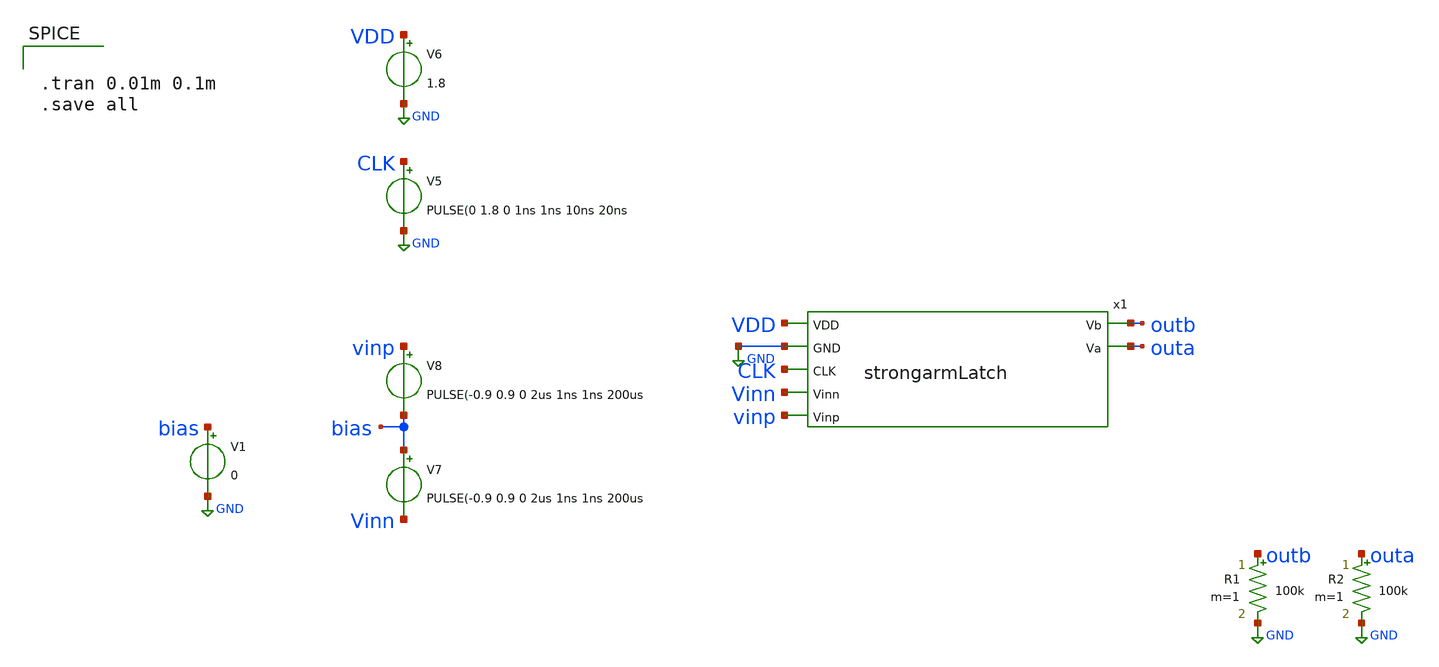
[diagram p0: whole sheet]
** sch_path: xschem/strongarmtb.sch
**.subckt strongarmtb
x1 outb outa VDD GND CLK Vinn vinp strongarmLatch
V5 CLK GND PULSE(0 1.8 0 1ns 1ns 10ns 20ns
V6 VDD GND 1.8
V7 bias Vinn PULSE(-0.9 0.9 0 2us 1ns 1ns 200us
V8 vinp bias PULSE(-0.9 0.9 0 2us 1ns 1ns 200us
V1 bias GND 0
R1 outb GND 100k m=1
R2 outa GND 100k m=1
**** begin user architecture code


.tran 0.01m 0.1m
.save all



** opencircuitdesign pdks install
.lib $::SKYWATER_MODELS/sky130.lib.spice tt


**** end user architecture code
**.ends
.GLOBAL GND
.end
